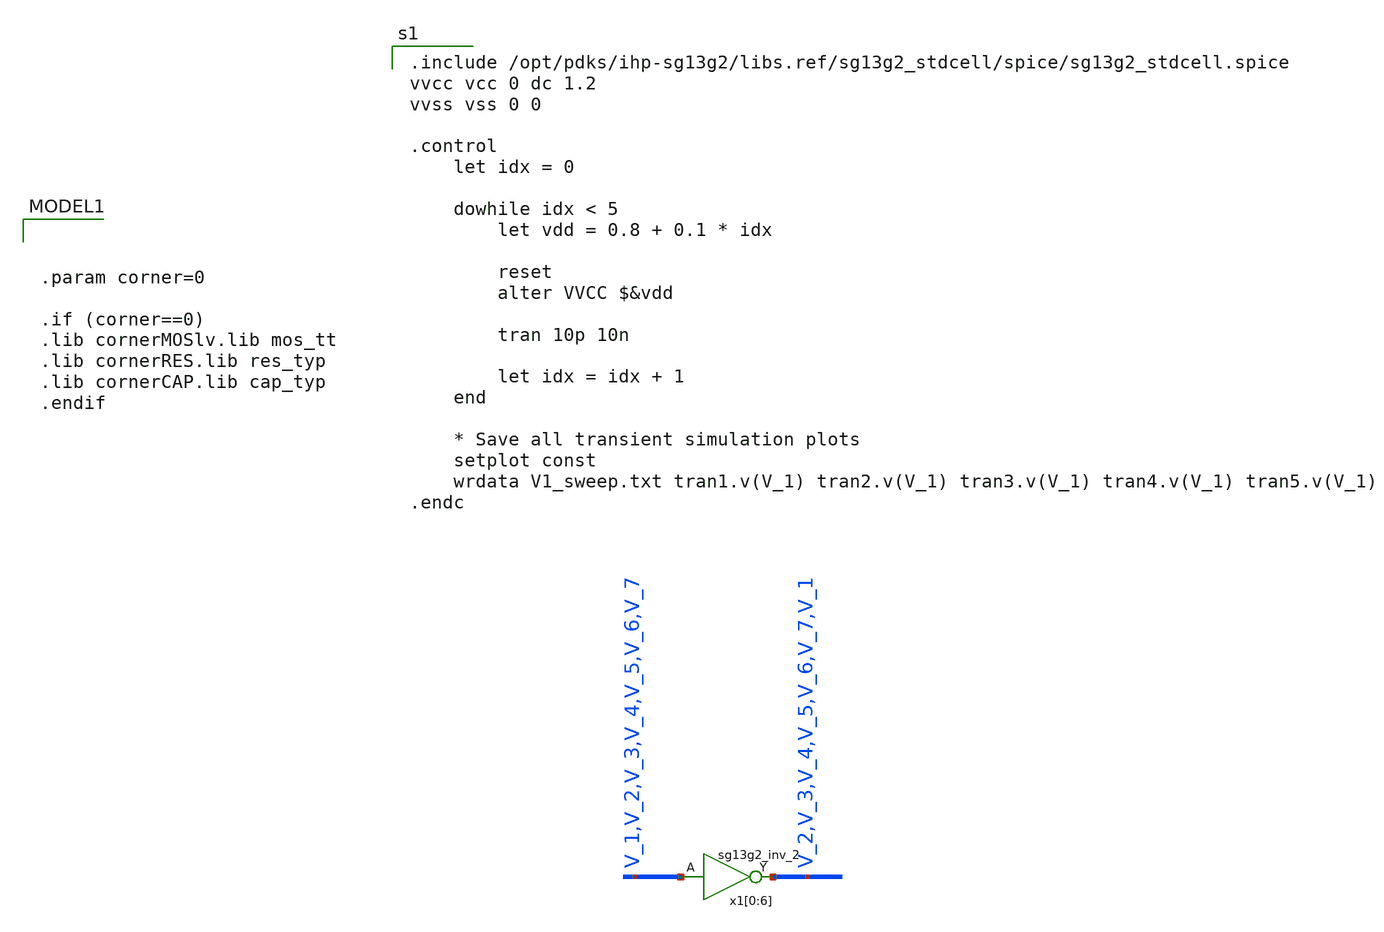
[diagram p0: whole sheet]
** sch_path: Day1/tb_7stage_VCRO_notation.sch
* IHP-GmbH/IHP-Open-PDK/ihp-sg13g2/libs.tech/xschem/sg13g2_stdcells/sg13g2_inv_2.sch:
* Copyright 2023 IHP PDK Authors
* Licensed under the Apache License, Version 2.0 (the "License");
**.subckt tb_7stage_VCRO_notation
x1[0] V_2 V_1 VCC VSS sg13g2_inv_2
x1[1] V_3 V_2 VCC VSS sg13g2_inv_2
x1[2] V_4 V_3 VCC VSS sg13g2_inv_2
x1[3] V_5 V_4 VCC VSS sg13g2_inv_2
x1[4] V_6 V_5 VCC VSS sg13g2_inv_2
x1[5] V_7 V_6 VCC VSS sg13g2_inv_2
x1[6] V_1 V_7 VCC VSS sg13g2_inv_2
**** begin user architecture code

.include /opt/pdks/ihp-sg13g2/libs.ref/sg13g2_stdcell/spice/sg13g2_stdcell.spice
vvcc vcc 0 dc 1.2
vvss vss 0 0

.control
    let idx = 0

    dowhile idx < 5
        let vdd = 0.8 + 0.1 * idx

        reset
        alter VVCC $&vdd

        tran 10p 10n

        let idx = idx + 1
    end

    * Save all transient simulation plots
    setplot const
    wrdata V1_sweep.txt tran1.v(V_1) tran2.v(V_1) tran3.v(V_1) tran4.v(V_1) tran5.v(V_1)
.endc




.param corner=0

.if (corner==0)
.lib cornerMOSlv.lib mos_tt
.lib cornerRES.lib res_typ
.lib cornerCAP.lib cap_typ
.endif

**** end user architecture code
**.ends

* expanding   symbol:  sg13g2_inv_2.sym # of pins=2
** sym_path: sg13g2_inv_2.sym
** sch_path: sg13g2_inv_2.sch
.subckt sg13g2_inv_2 Y A VDD VSS
*.opin Y
*.ipin A
*.iopin VDD
*.iopin VSS
XM1 Y A VSS VSS sg13_lv_nmos w=1.48u l=130.00n ng=2 m=1 mm_ok=1
XM2 Y A VDD VDD sg13_lv_pmos w=2.24u l=130.00n ng=2 m=1 mm_ok=1
.ends

.end
